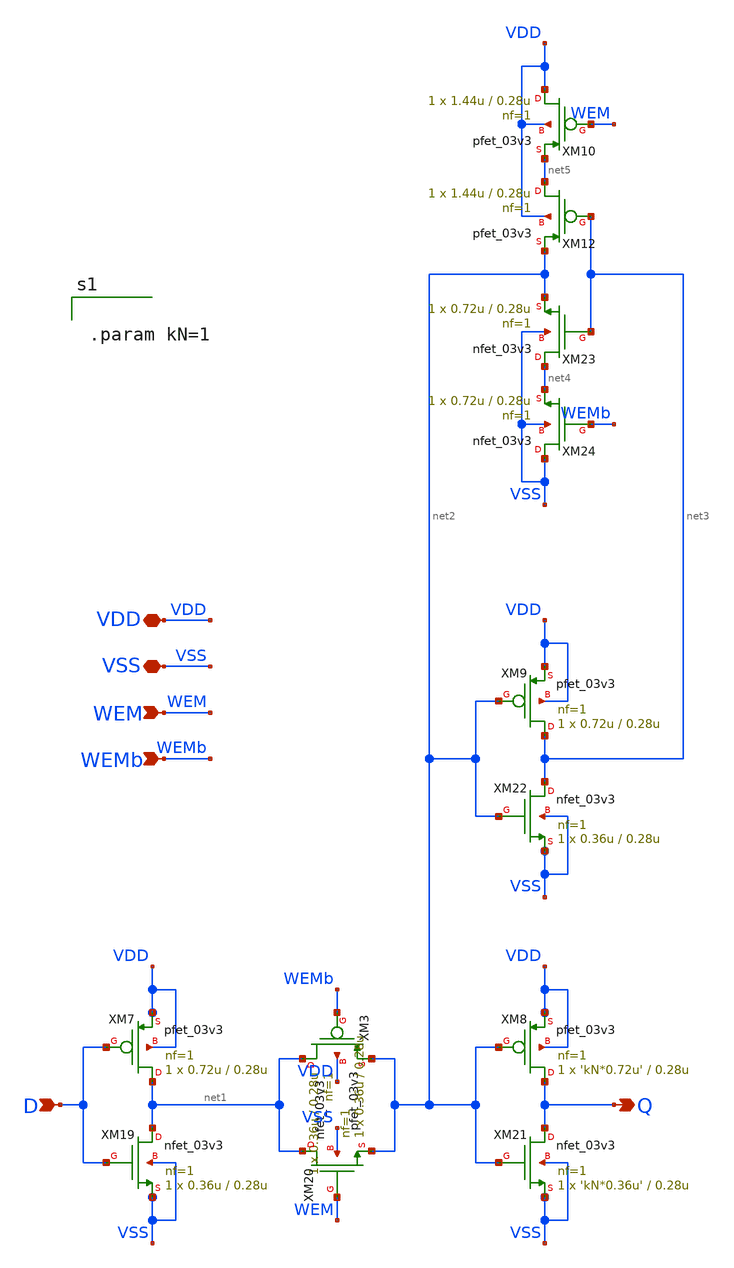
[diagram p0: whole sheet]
** sch_path: CAD3/master_latch.sch
**.subckt master_latch D WEMb WEM VSS VDD Q
*.ipin D
*.ipin WEMb
*.ipin WEM
*.iopin VSS
*.iopin VDD
*.opin Q
XM3 net1 WEMb net2 VDD pfet_03v3 L=0.28u W=0.36u nf=1 ad='int((nf+1)/2) * W/nf * 0.18u' as='int((nf+2)/2) * W/nf * 0.18u'
+ pd='2*int((nf+1)/2) * (W/nf + 0.18u)' ps='2*int((nf+2)/2) * (W/nf + 0.18u)' nrd='0.18u / W' nrs='0.18u / W'
+ sa=0 sb=0 sd=0 m=1
XM7 net1 D VDD VDD pfet_03v3 L=0.28u W=0.72u nf=1 ad='int((nf+1)/2) * W/nf * 0.18u' as='int((nf+2)/2) * W/nf * 0.18u'
+ pd='2*int((nf+1)/2) * (W/nf + 0.18u)' ps='2*int((nf+2)/2) * (W/nf + 0.18u)' nrd='0.18u / W' nrs='0.18u / W'
+ sa=0 sb=0 sd=0 m=1
XM8 Q net2 VDD VDD pfet_03v3 L=0.28u W='kN*0.72u' nf=1 ad='int((nf+1)/2) * W/nf * 0.18u' as='int((nf+2)/2) * W/nf * 0.18u'
+ pd='2*int((nf+1)/2) * (W/nf + 0.18u)' ps='2*int((nf+2)/2) * (W/nf + 0.18u)' nrd='0.18u / W' nrs='0.18u / W'
+ sa=0 sb=0 sd=0 m=1
XM9 net3 net2 VDD VDD pfet_03v3 L=0.28u W=0.72u nf=1 ad='int((nf+1)/2) * W/nf * 0.18u' as='int((nf+2)/2) * W/nf * 0.18u'
+ pd='2*int((nf+1)/2) * (W/nf + 0.18u)' ps='2*int((nf+2)/2) * (W/nf + 0.18u)' nrd='0.18u / W' nrs='0.18u / W'
+ sa=0 sb=0 sd=0 m=1
XM10 VDD WEM net5 VDD pfet_03v3 L=0.28u W=1.44u nf=1 ad='int((nf+1)/2) * W/nf * 0.18u' as='int((nf+2)/2) * W/nf * 0.18u'
+ pd='2*int((nf+1)/2) * (W/nf + 0.18u)' ps='2*int((nf+2)/2) * (W/nf + 0.18u)' nrd='0.18u / W' nrs='0.18u / W'
+ sa=0 sb=0 sd=0 m=1
XM12 net5 net3 net2 VDD pfet_03v3 L=0.28u W=1.44u nf=1 ad='int((nf+1)/2) * W/nf * 0.18u' as='int((nf+2)/2) * W/nf * 0.18u'
+ pd='2*int((nf+1)/2) * (W/nf + 0.18u)' ps='2*int((nf+2)/2) * (W/nf + 0.18u)' nrd='0.18u / W' nrs='0.18u / W'
+ sa=0 sb=0 sd=0 m=1
XM19 net1 D VSS VSS nfet_03v3 L=0.28u W=0.36u nf=1 ad='int((nf+1)/2) * W/nf * 0.18u' as='int((nf+2)/2) * W/nf * 0.18u'
+ pd='2*int((nf+1)/2) * (W/nf + 0.18u)' ps='2*int((nf+2)/2) * (W/nf + 0.18u)' nrd='0.18u / W' nrs='0.18u / W'
+ sa=0 sb=0 sd=0 m=1
XM20 net1 WEM net2 VSS nfet_03v3 L=0.28u W=0.36u nf=1 ad='int((nf+1)/2) * W/nf * 0.18u' as='int((nf+2)/2) * W/nf * 0.18u'
+ pd='2*int((nf+1)/2) * (W/nf + 0.18u)' ps='2*int((nf+2)/2) * (W/nf + 0.18u)' nrd='0.18u / W' nrs='0.18u / W'
+ sa=0 sb=0 sd=0 m=1
XM21 Q net2 VSS VSS nfet_03v3 L=0.28u W='kN*0.36u' nf=1 ad='int((nf+1)/2) * W/nf * 0.18u' as='int((nf+2)/2) * W/nf * 0.18u'
+ pd='2*int((nf+1)/2) * (W/nf + 0.18u)' ps='2*int((nf+2)/2) * (W/nf + 0.18u)' nrd='0.18u / W' nrs='0.18u / W'
+ sa=0 sb=0 sd=0 m=1
XM22 net3 net2 VSS VSS nfet_03v3 L=0.28u W=0.36u nf=1 ad='int((nf+1)/2) * W/nf * 0.18u' as='int((nf+2)/2) * W/nf * 0.18u'
+ pd='2*int((nf+1)/2) * (W/nf + 0.18u)' ps='2*int((nf+2)/2) * (W/nf + 0.18u)' nrd='0.18u / W' nrs='0.18u / W'
+ sa=0 sb=0 sd=0 m=1
XM23 net4 net3 net2 VSS nfet_03v3 L=0.28u W=0.72u nf=1 ad='int((nf+1)/2) * W/nf * 0.18u' as='int((nf+2)/2) * W/nf * 0.18u'
+ pd='2*int((nf+1)/2) * (W/nf + 0.18u)' ps='2*int((nf+2)/2) * (W/nf + 0.18u)' nrd='0.18u / W' nrs='0.18u / W'
+ sa=0 sb=0 sd=0 m=1
XM24 VSS WEMb net4 VSS nfet_03v3 L=0.28u W=0.72u nf=1 ad='int((nf+1)/2) * W/nf * 0.18u' as='int((nf+2)/2) * W/nf * 0.18u'
+ pd='2*int((nf+1)/2) * (W/nf + 0.18u)' ps='2*int((nf+2)/2) * (W/nf + 0.18u)' nrd='0.18u / W' nrs='0.18u / W'
+ sa=0 sb=0 sd=0 m=1
**** begin user architecture code


.param kN=1


**** end user architecture code
**.ends
.end
